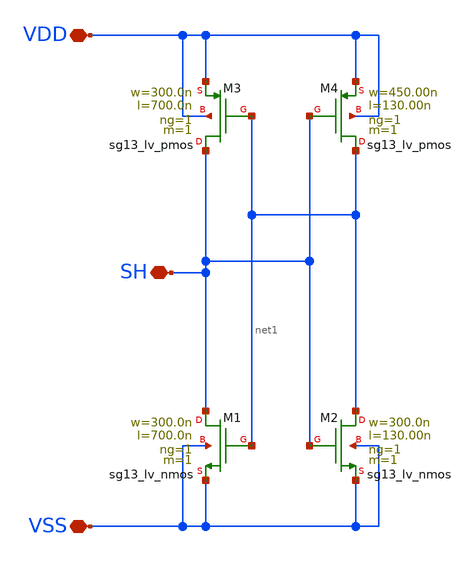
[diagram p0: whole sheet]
** sch_path: ihp-sg13g2/libs.tech/xschem/sg13g2_stdcells/sg13g2_sighold.sch
**.subckt sg13g2_sighold VDD VSS SH
*.iopin VDD
*.iopin VSS
*.iopin SH
XM1 SH net1 VSS VSS sg13_lv_nmos w=300.0n l=700.0n ng=1 m=1 mm_ok=1
XM2 net1 SH VSS VSS sg13_lv_nmos w=300.0n l=130.00n ng=1 m=1 mm_ok=1
XM3 SH net1 VDD VDD sg13_lv_pmos w=300.0n l=700.0n ng=1 m=1 mm_ok=1
XM4 net1 SH VDD VDD sg13_lv_pmos w=450.00n l=130.00n ng=1 m=1 mm_ok=1
**.ends
.end
